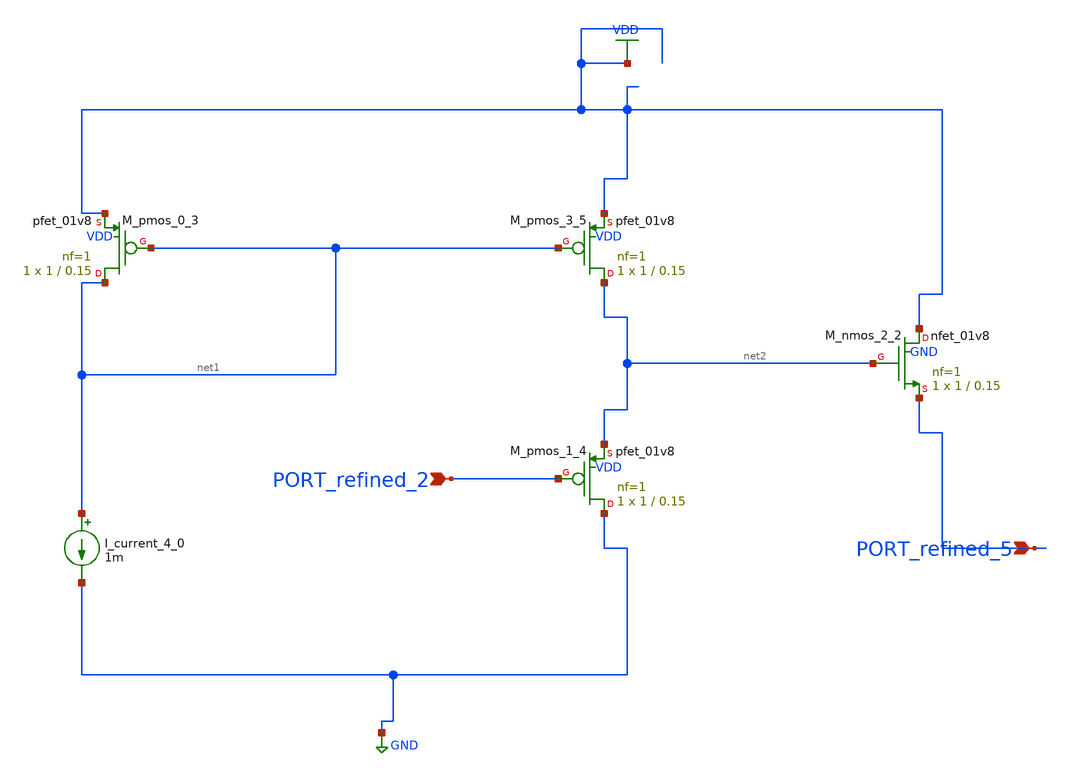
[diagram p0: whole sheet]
** sch_path: schematics/10_1587_elex_XX_XXXXXXXX_04_001.sch
**.subckt 10_1587_elex_XX_XXXXXXXX_04_001 PORT_refined_5 PORT_refined_2
*.ipin PORT_refined_5
*.ipin PORT_refined_2
I_current_4_0 net1 GND 1m
XM_nmos_2_2 VDD net2 PORT_refined_5 GND sky130_fd_pr__nfet_01v8 L=0.15 W=1 nf=1 ad='int((1 + 1)/2) * 1 / 1 * 0.29'
+ as='int((1 + 2)/2) * 1 / 1 * 0.29' pd='2*int((1 + 1)/2) * (1 / 1 + 0.29)' ps='2*int((1 + 2)/2) * (1 / 1 + 0.29)'
+ nrd='0.29 / 1 ' nrs='0.29 / 1 ' sa=0 sb=0 sd=0 mult=1 m=1
XM_pmos_0_3 net1 net1 VDD VDD sky130_fd_pr__pfet_01v8 L=0.15 W=1 nf=1 ad='int((1 + 1)/2) * 1 / 1 * 0.29'
+ as='int((1 + 2)/2) * 1 / 1 * 0.29' pd='2*int((1 + 1)/2) * (1 / 1 + 0.29)' ps='2*int((1 + 2)/2) * (1 / 1 + 0.29)'
+ nrd='0.29 / 1 ' nrs='0.29 / 1 ' sa=0 sb=0 sd=0 mult=1 m=1
XM_pmos_1_4 GND PORT_refined_2 net2 VDD sky130_fd_pr__pfet_01v8 L=0.15 W=1 nf=1 ad='int((1 + 1)/2) * 1 / 1 * 0.29'
+ as='int((1 + 2)/2) * 1 / 1 * 0.29' pd='2*int((1 + 1)/2) * (1 / 1 + 0.29)' ps='2*int((1 + 2)/2) * (1 / 1 + 0.29)'
+ nrd='0.29 / 1 ' nrs='0.29 / 1 ' sa=0 sb=0 sd=0 mult=1 m=1
XM_pmos_3_5 net2 net1 VDD VDD sky130_fd_pr__pfet_01v8 L=0.15 W=1 nf=1 ad='int((1 + 1)/2) * 1 / 1 * 0.29'
+ as='int((1 + 2)/2) * 1 / 1 * 0.29' pd='2*int((1 + 1)/2) * (1 / 1 + 0.29)' ps='2*int((1 + 2)/2) * (1 / 1 + 0.29)'
+ nrd='0.29 / 1 ' nrs='0.29 / 1 ' sa=0 sb=0 sd=0 mult=1 m=1
**.ends
.GLOBAL GND
.GLOBAL VDD
.end
